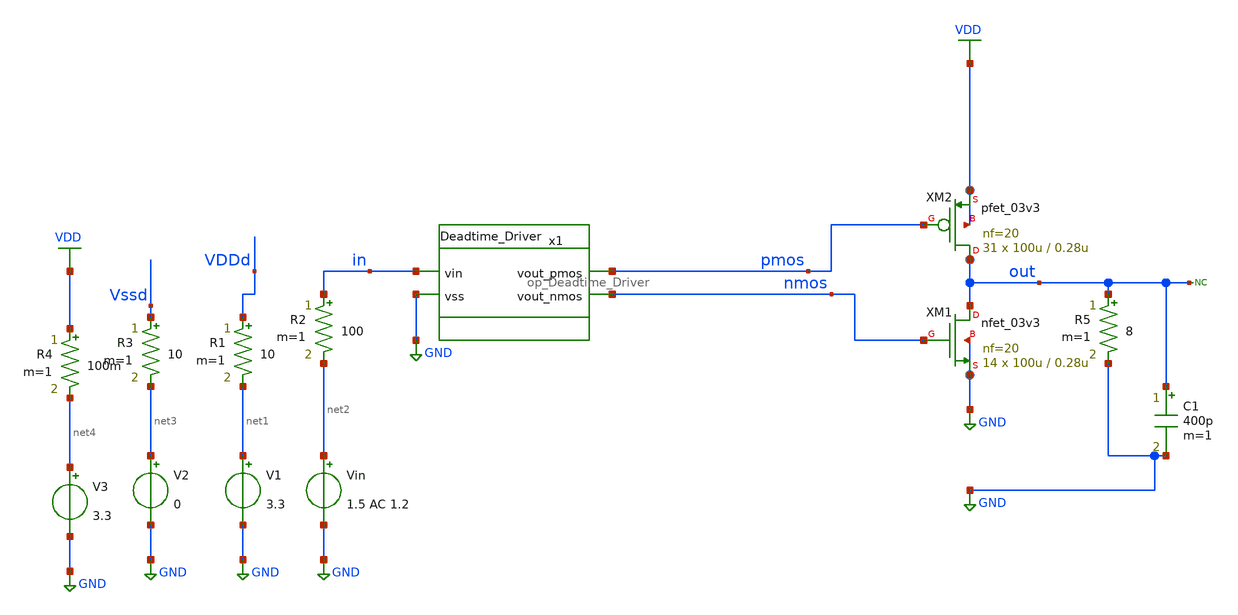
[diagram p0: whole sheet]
** sch_path: designs/libs/tb_analog/tb_op_Deadtime_Driver/tb_temp_deadtime_driver.sch
**.subckt tb_temp_deadtime_driver
V1 net1 GND 3.3
Vin net2 GND 1.5 AC 1.2
R1 VDDd net1 10 m=1
R2 in net2 100 m=1
V2 net3 GND 0
R3 Vssd net3 10 m=1
x1 pmos in nmos GND op_Deadtime_Driver
XM1 out nmos GND GND nfet_03v3 L=0.28u W=100u nf=20 ad='int((nf+1)/2) * W/nf * 0.18u' as='int((nf+2)/2) * W/nf * 0.18u'
+ pd='2*int((nf+1)/2) * (W/nf + 0.18u)' ps='2*int((nf+2)/2) * (W/nf + 0.18u)' nrd='0.18u / W' nrs='0.18u / W'
+ sa=0 sb=0 sd=0 m=14
XM2 out pmos VDD VDD pfet_03v3 L=0.28u W=100u nf=20 ad='int((nf+1)/2) * W/nf * 0.18u' as='int((nf+2)/2) * W/nf * 0.18u'
+ pd='2*int((nf+1)/2) * (W/nf + 0.18u)' ps='2*int((nf+2)/2) * (W/nf + 0.18u)' nrd='0.18u / W' nrs='0.18u / W'
+ sa=0 sb=0 sd=0 m=31
* noconn out
V3 net4 GND 3.3
R4 VDD net4 100m m=1
R5 out GND 8 m=1
C1 out GND 400p m=1
**** begin user architecture code

.include $::180MCU_MODELS/design.ngspice
.include /foss/pdks/gf180mcuD/libs.ref/gf180mcu_fd_sc_mcu9t5v0/spice/gf180mcu_fd_sc_mcu9t5v0.spice
.lib $::180MCU_MODELS/sm141064.ngspice typical
.lib $::180MCU_MODELS/sm141064.ngspice cap_mim
.lib $::180MCU_MODELS/sm141064.ngspice mimcap_typical



.temp -40
.options savecurrents
.global VDDd VSSd
.control
save all
**Frequency & time settings
let fsig = 200k
let tper=1/fsig
let tfr = 0.01*tper
let ton = 0.5*tper-2*tfr

let tstop = 4 * tper
let tstep = 0.001*tper


**voltages
alter @Vin[PULSE] = [ 0 2.3 0 $&tfr $&tfr $&ton $&tper 3 ]
alter @Vin[DC] = 3.3
*alter @Vin[SIN] = [ 1.7 1.5 $&fsig 0 0 ]

**simulation
OP
*show all > op.log
show all

**Temperature analysis
tran $&tstep $&tstop
let t = $temp
print t
*plot nmos pmos
plot out
meas tran tfall_p WHEN v(pmos)=0.68 FALL=3
meas tran tfall_n WHEN v(nmos)=0.68 FALL=3

meas tran trise_p WHEN v(pmos)=0.68 RISE=3
meas tran trise_n WHEN v(nmos)=0.68 RISE=3

let delay_fall = $&tfall_p - $&tfall_n
let delay_rise = $&trise_p - $&trise_n

print delay_fall
print delay_rise

**check shoot-through
plot @r5[i] v3#branch @m.xm1.m0[id]
plot @m.xm1.m0[id]
write Deadtime_Driver_temp_tb.txt
.endc


**** end user architecture code
**.ends
.GLOBAL GND
.GLOBAL VDD
.end
